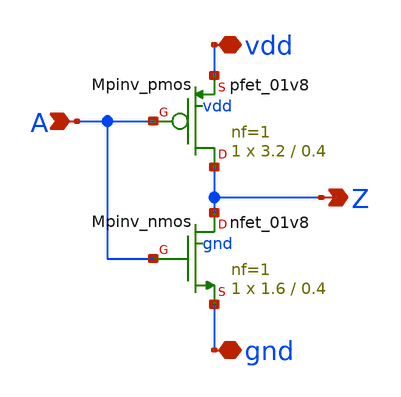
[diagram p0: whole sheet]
** sch_path: sram_2_16_scn4m/pinv_10.sch
**.subckt pinv_10 A Z vdd gnd
*.ipin A
*.opin Z
*.iopin vdd
*.iopin gnd
XMpinv_nmos Z A gnd gnd sky130_fd_pr__nfet_01v8 L=0.4 W=1.6 nf=1 ad='int((nf+1)/2) * W/nf * 0.29' as='int((nf+2)/2) * W/nf * 0.29'
+ pd='2*int((nf+1)/2) * (W/nf + 0.29)' ps='2*int((nf+2)/2) * (W/nf + 0.29)' nrd='0.29 / W' nrs='0.29 / W'
+ sa=0 sb=0 sd=0 mult=1 m=1
XMpinv_pmos Z A vdd vdd sky130_fd_pr__pfet_01v8 L=0.4 W=3.2 nf=1 ad='int((nf+1)/2) * W/nf * 0.29' as='int((nf+2)/2) * W/nf * 0.29'
+ pd='2*int((nf+1)/2) * (W/nf + 0.29)' ps='2*int((nf+2)/2) * (W/nf + 0.29)' nrd='0.29 / W' nrs='0.29 / W'
+ sa=0 sb=0 sd=0 mult=1 m=1
**.ends
.end
